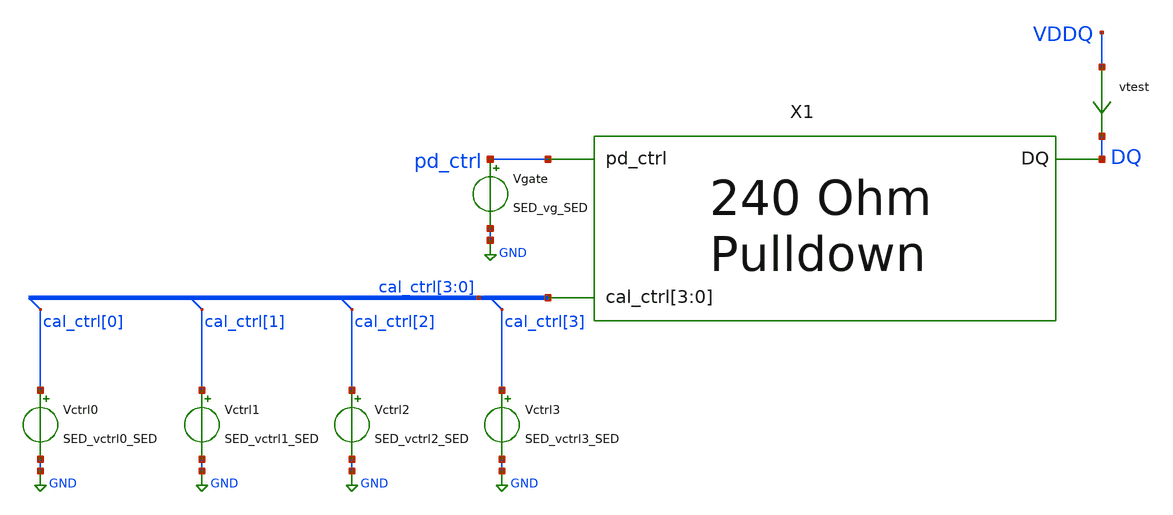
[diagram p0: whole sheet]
** sch_path: n-leg_tb.sch
* Copyright 2021 Stefan Frederik Schippers
* Licensed under the Apache License, Version 2.0 (the "License");
* you may not use this file except in compliance with the License.
* You may obtain a copy of the License at
* https://www.apache.org/licenses/LICENSE-2.0
* Unless required by applicable law or agreed to in writing, software
* distributed under the License is distributed on an "AS IS" BASIS,
* WITHOUT WARRANTIES OR CONDITIONS OF ANY KIND, either express or implied.
* See the License for the specific language governing permissions and
* limitations under the License.
**.subckt n-leg_tb
vtest VDDQ DQ 0
.save i(vtest)
Vgate pd_ctrl GND SED_vg_SED
Vctrl0 cal_ctrl[0] GND SED_vctrl0_SED
Vctrl1 cal_ctrl[1] GND SED_vctrl1_SED
Vctrl2 cal_ctrl[2] GND SED_vctrl2_SED
Vctrl3 cal_ctrl[3] GND SED_vctrl3_SED
X1 DQ pd_ctrl cal_ctrl[3] cal_ctrl[2] cal_ctrl[1] cal_ctrl[0] n-leg
**** begin user architecture code
 ** Local library links to pdk
.lib ./libs/SED_process_SED_lib.spice SED_process_SED

**** end user architecture code
**.ends

* expanding   symbol:  /mnt/users/ssd2/homes/hinesd3/proj/n-leg-design/n-leg.sym # of pins=3
** sym_path: schem/n-leg.sym
** sch_path: schem/n-leg.sch
.subckt n-leg DQ pd_ctrl cal_ctrl[3] cal_ctrl[2] cal_ctrl[1] cal_ctrl[0]
*.iopin DQ
*.ipin pd_ctrl
*.ipin cal_ctrl[3],cal_ctrl[2],cal_ctrl[1],cal_ctrl[0]
XR1 vpulldown net1 sky130_fd_pr__res_generic_po W=0.33 L=1.7 m=1
Xn1 vpulldown net2 GND GND sky130_fd_pr__nfet_01v8 L=0.15 W=0.65 nf=1 ad='int((nf+1)/2) * W/nf * 0.29'
+ as='int((nf+2)/2) * W/nf * 0.29' pd='2*int((nf+1)/2) * (W/nf + 0.29)' ps='2*int((nf+2)/2) * (W/nf + 0.29)'
+ nrd='0.29 / W' nrs='0.29 / W' sa=0 sb=0 sd=0 mult=48 m=48
Xnctrl0 net1 cal_ctrl[0] vpulldown GND sky130_fd_pr__nfet_01v8 L=0.15 W=0.65 nf=1 ad='int((nf+1)/2) * W/nf * 0.29'
+ as='int((nf+2)/2) * W/nf * 0.29' pd='2*int((nf+1)/2) * (W/nf + 0.29)' ps='2*int((nf+2)/2) * (W/nf + 0.29)'
+ nrd='0.29 / W' nrs='0.29 / W' sa=0 sb=0 sd=0 mult=32 m=32
Xnctrl1 net1 cal_ctrl[1] vpulldown GND sky130_fd_pr__nfet_01v8 L=0.15 W=0.65 nf=1 ad='int((nf+1)/2) * W/nf * 0.29'
+ as='int((nf+2)/2) * W/nf * 0.29' pd='2*int((nf+1)/2) * (W/nf + 0.29)' ps='2*int((nf+2)/2) * (W/nf + 0.29)'
+ nrd='0.29 / W' nrs='0.29 / W' sa=0 sb=0 sd=0 mult=8 m=8
Xnctrl2 net1 cal_ctrl[2] vpulldown GND sky130_fd_pr__nfet_01v8 L=0.15 W=0.975 nf=1 ad='int((nf+1)/2) * W/nf * 0.29'
+ as='int((nf+2)/2) * W/nf * 0.29' pd='2*int((nf+1)/2) * (W/nf + 0.29)' ps='2*int((nf+2)/2) * (W/nf + 0.29)'
+ nrd='0.29 / W' nrs='0.29 / W' sa=0 sb=0 sd=0 mult=2 m=2
Xnctrl3 net1 cal_ctrl[3] vpulldown GND sky130_fd_pr__nfet_01v8 L=0.15 W=0.5 nf=1 ad='int((nf+1)/2) * W/nf * 0.29'
+ as='int((nf+2)/2) * W/nf * 0.29' pd='2*int((nf+1)/2) * (W/nf + 0.29)' ps='2*int((nf+2)/2) * (W/nf + 0.29)'
+ nrd='0.29 / W' nrs='0.29 / W' sa=0 sb=0 sd=0 mult=1 m=1
Xnctrl_tot GND GND GND GND sky130_fd_pr__nfet_01v8 L=0.15 W=0.65 nf=1 ad='int((nf+1)/2) * W/nf * 0.29'
+ as='int((nf+2)/2) * W/nf * 0.29' pd='2*int((nf+1)/2) * (W/nf + 0.29)' ps='2*int((nf+2)/2) * (W/nf + 0.29)'
+ nrd='0.29 / W' nrs='0.29 / W' sa=0 sb=0 sd=0 mult=11 m=11
Vcur_out DQ net1 0
.save i(vcur_out)
Vcur_in pd_ctrl net2 0
.save i(vcur_in)
.ends

.GLOBAL GND
**** begin user architecture code



* power voltage
vvddq VDDQ 0 0
*.param rwidth=4.6

.control
save all
set temp=SED_temp_SED

* RUN SIMULATION
dc vvddq 0.3 1.2 0.05
* OUTPUT
print v(vddq)/i(vtest)
wrdata out/data/SED_plotName_SED.txt v(vddq)/i(vtest)
set hcopydevtype = svg
hardcopy ./out/plots/SED_plotName_SED.svg vddq/I(vtest) vs vddq title 'Resistance vs pin voltage'

.endc


**** end user architecture code
.end
